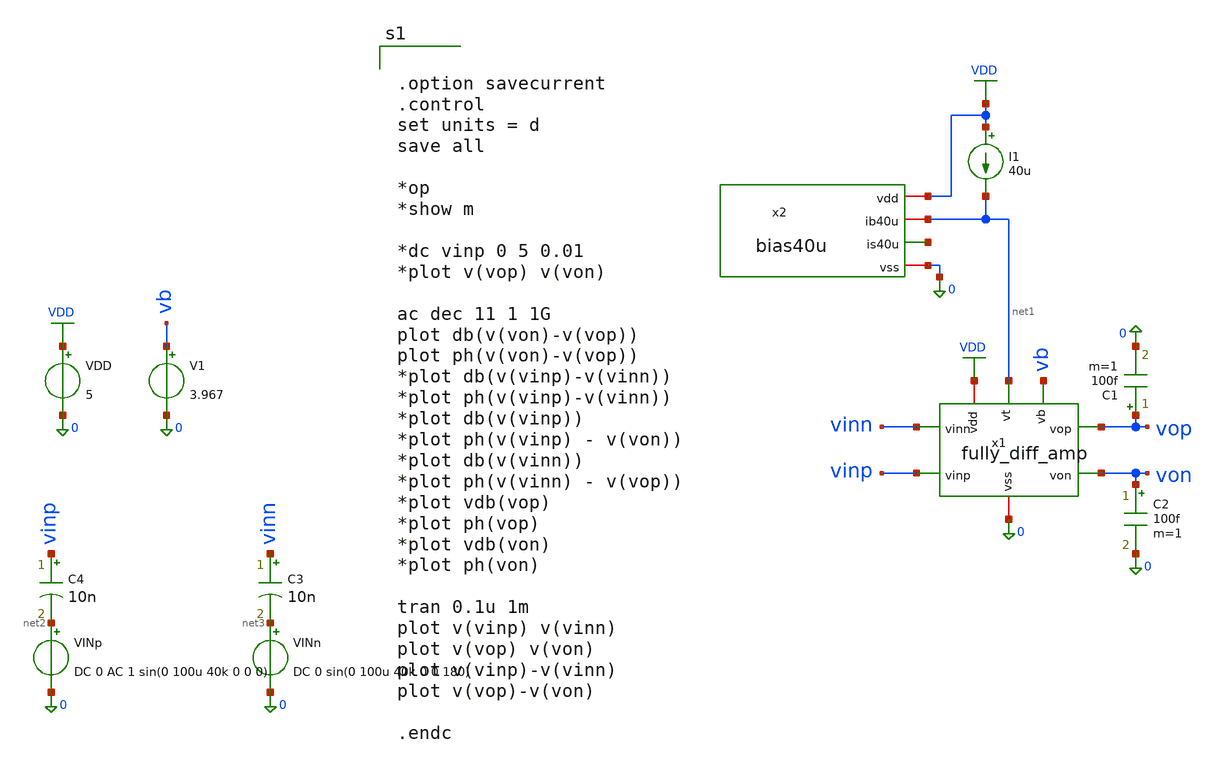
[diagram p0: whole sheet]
** sch_path: member_project/JJY_Receiver/Masahiro/jjy_recv/diff_amp/diff_amp_single_out.sch
**.subckt diff_amp_single_out
VDD VDD 0 5
VINp net2 0 DC 0 AC 1 sin(0 100u 40k 0 0 0)
V1 vb 0 3.967
VINn net3 0 DC 0 sin(0 100u 40k 0 0 180)
C3 vinn net3 10n m=1
C4 vinp net2 10n m=1
C1 vop 0 100f m=1
I1 VDD net1 40u
x1 vb VDD vop von 0 vinn vinp net1 fully_diff_amp
C2 von 0 100f m=1
x2 VDD net1 net4 0 bias40u
**** begin user architecture code
 .include $::LIB/ip62_models


.option savecurrent
.control
set units = d
save all

*op
*show m

*dc vinp 0 5 0.01
*plot v(vop) v(von)

ac dec 11 1 1G
plot db(v(von)-v(vop))
plot ph(v(von)-v(vop))
*plot db(v(vinp)-v(vinn))
*plot ph(v(vinp)-v(vinn))
*plot db(v(vinp))
*plot ph(v(vinp) - v(von))
*plot db(v(vinn))
*plot ph(v(vinn) - v(vop))
*plot vdb(vop)
*plot ph(vop)
*plot vdb(von)
*plot ph(von)

tran 0.1u 1m
plot v(vinp) v(vinn)
plot v(vop) v(von)
plot v(vinp)-v(vinn)
plot v(vop)-v(von)

.endc


**** end user architecture code
**.ends

* expanding   symbol:  fully_diff_amp.sym # of pins=8
** sym_path: member_project/JJY_Receiver/Masahiro/jjy_recv/diff_amp/fully_diff_amp.sym
** sch_path: member_project/JJY_Receiver/Masahiro/jjy_recv/diff_amp/fully_diff_amp.sch
.subckt fully_diff_amp vb vdd vop von vss vinn vinp vt
*.opin vop
*.opin von
*.ipin vinp
*.ipin vb
*.ipin vt
*.ipin vinn
*.iopin vdd
*.iopin vss
XM1 vop vb vdd vdd PMOS w=45u l=2u as=0 ad=0 ps=0 pd=0 nrd=0 nrs=0 m=1
XM2 von vb vdd vdd PMOS w=45u l=2u as=0 ad=0 ps=0 pd=0 nrd=0 nrs=0 m=1
XM3 net1 vt vss vss NMOS w=10u l=2u as=0 ad=0 ps=0 pd=0 nrd=0 nrs=0 m=2
XM7 von vinp net1 vss NMOS w=20u l=2u as=0 ad=0 ps=0 pd=0 nrd=0 nrs=0 m=1
XM8 vop vinn net1 vss NMOS w=20u l=2u as=0 ad=0 ps=0 pd=0 nrd=0 nrs=0 m=1
XM6 net2 net2 vop vdd PMOS w=45u l=8u as=0 ad=0 ps=0 pd=0 nrd=0 nrs=0 m=1
XM9 net2 net2 vinn vdd PMOS w=45u l=8u as=0 ad=0 ps=0 pd=0 nrd=0 nrs=0 m=1
XM5 net3 net3 von vdd PMOS w=45u l=8u as=0 ad=0 ps=0 pd=0 nrd=0 nrs=0 m=1
XM10 net3 net3 vinp vdd PMOS w=45u l=8u as=0 ad=0 ps=0 pd=0 nrd=0 nrs=0 m=1
XM12 vinn vinn vss vss NMOS w=12.6u l=8u as=0 ad=0 ps=0 pd=0 nrd=0 nrs=0 m=1
XM13 vinn vinn vdd vdd PMOS w=34.4u l=8u as=0 ad=0 ps=0 pd=0 nrd=0 nrs=0 m=1
XM11 vinp vinp vss vss NMOS w=12.6u l=8u as=0 ad=0 ps=0 pd=0 nrd=0 nrs=0 m=1
XM14 vinp vinp vdd vdd PMOS w=34.4u l=8u as=0 ad=0 ps=0 pd=0 nrd=0 nrs=0 m=1
.ends


* expanding   symbol:
*+  /home/ishi-kai/ISHI-KAI_Multiple_Projects_OpenMPW_OpenSUSI-TR10-1/member_project/JJY_Receiver/Masahiro/jjy_recv/bias_for_mix_amp/bias40u.sym # of pins=4
** sym_path: member_project/JJY_Receiver/Masahiro/jjy_recv/bias_for_mix_amp/bias40u.sym
** sch_path: member_project/JJY_Receiver/Masahiro/jjy_recv/bias_for_mix_amp/bias40u.sch
.subckt bias40u vdd ib40u is40u vss
*.iopin vss
*.iopin ib40u
*.iopin vdd
*.opin is40u
XXM1 ib40u ib40u vss vss NMOS w=10u l=2u nrd=0 nrs=0 m=2
XXM2 net1 ib40u vss vss NMOS w=10u l=2u nrd=0 nrs=0 m=2
XXM3 net1 vdd vdd vdd PMOS w=45u l=2u nrd=0 nrs=0 m=1
XXM4 is40u vdd vdd vdd PMOS w=45u l=2u nrd=0 nrs=0 m=1
.ends

.GLOBAL VDD
.end
